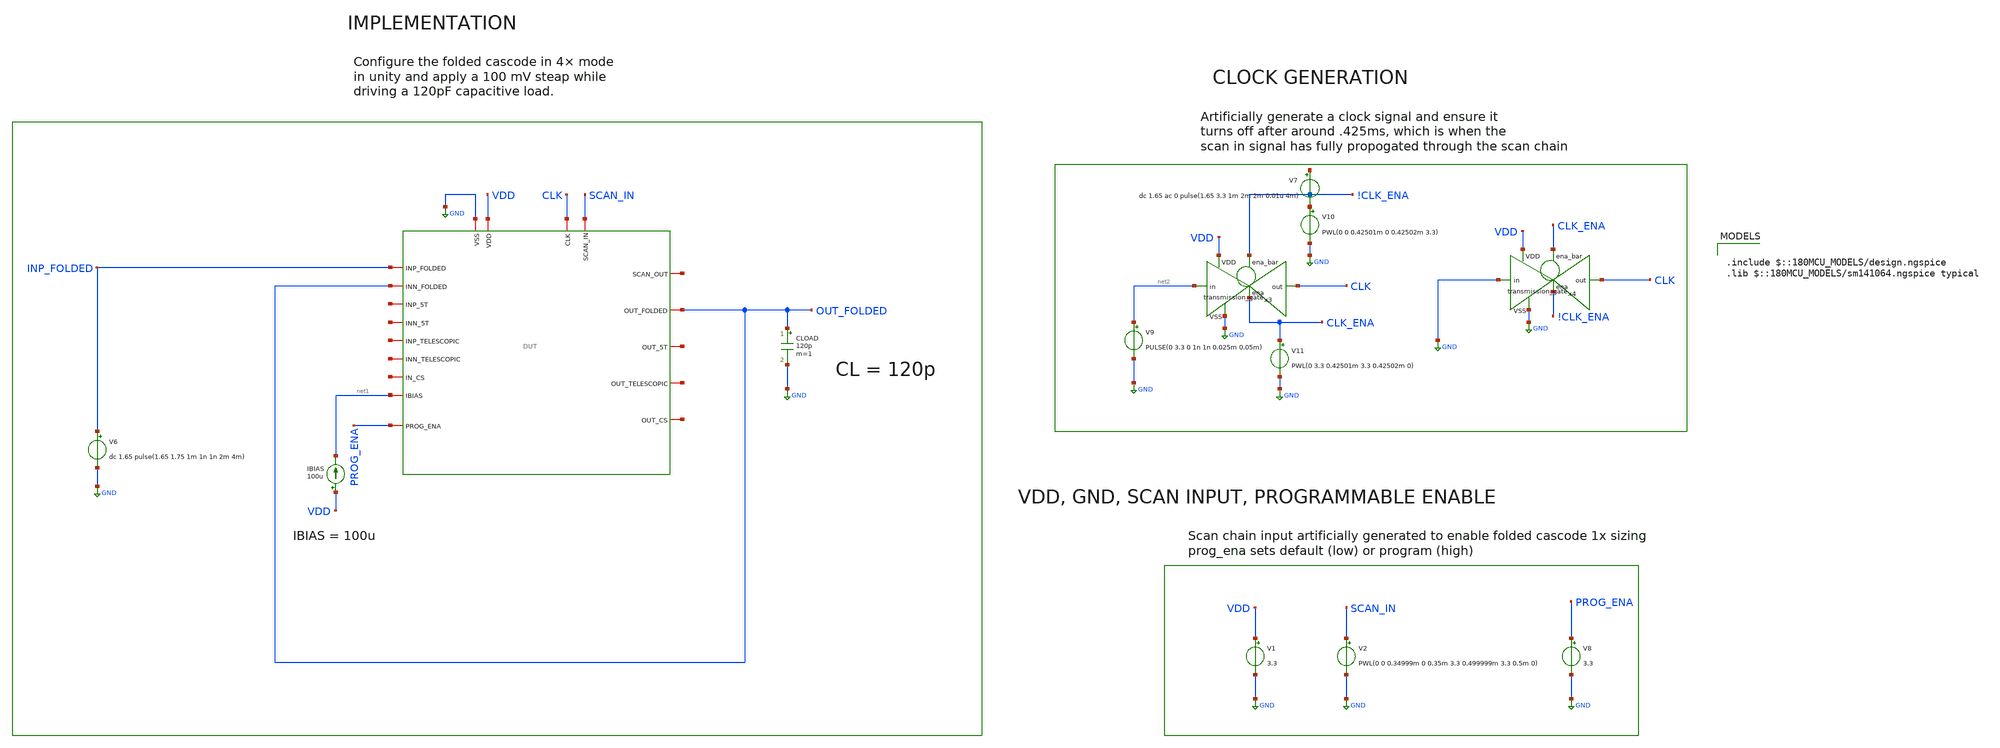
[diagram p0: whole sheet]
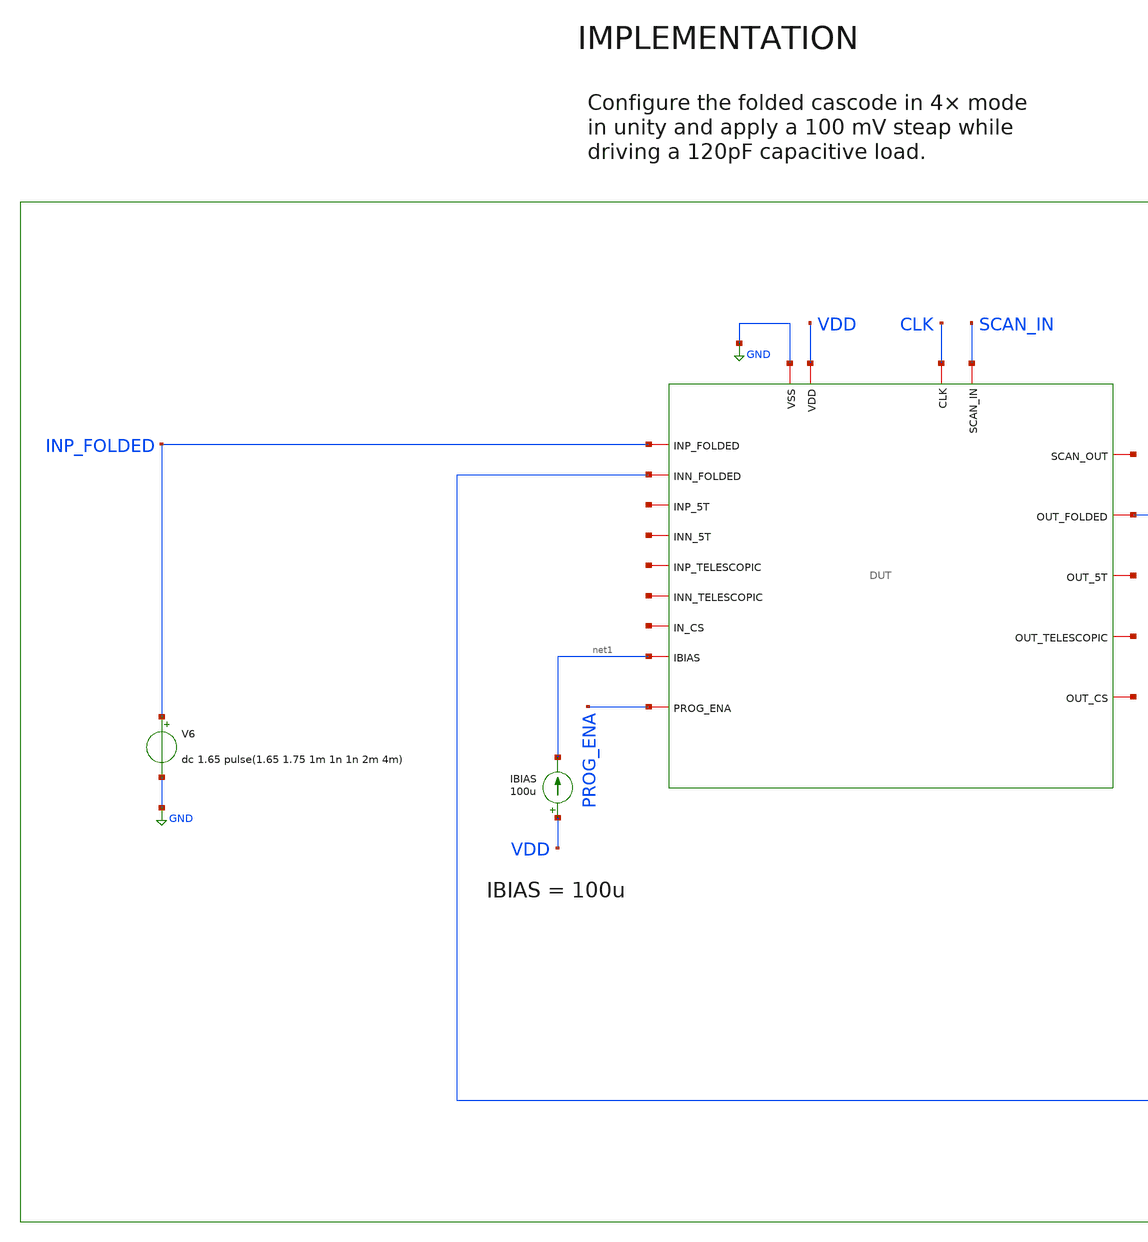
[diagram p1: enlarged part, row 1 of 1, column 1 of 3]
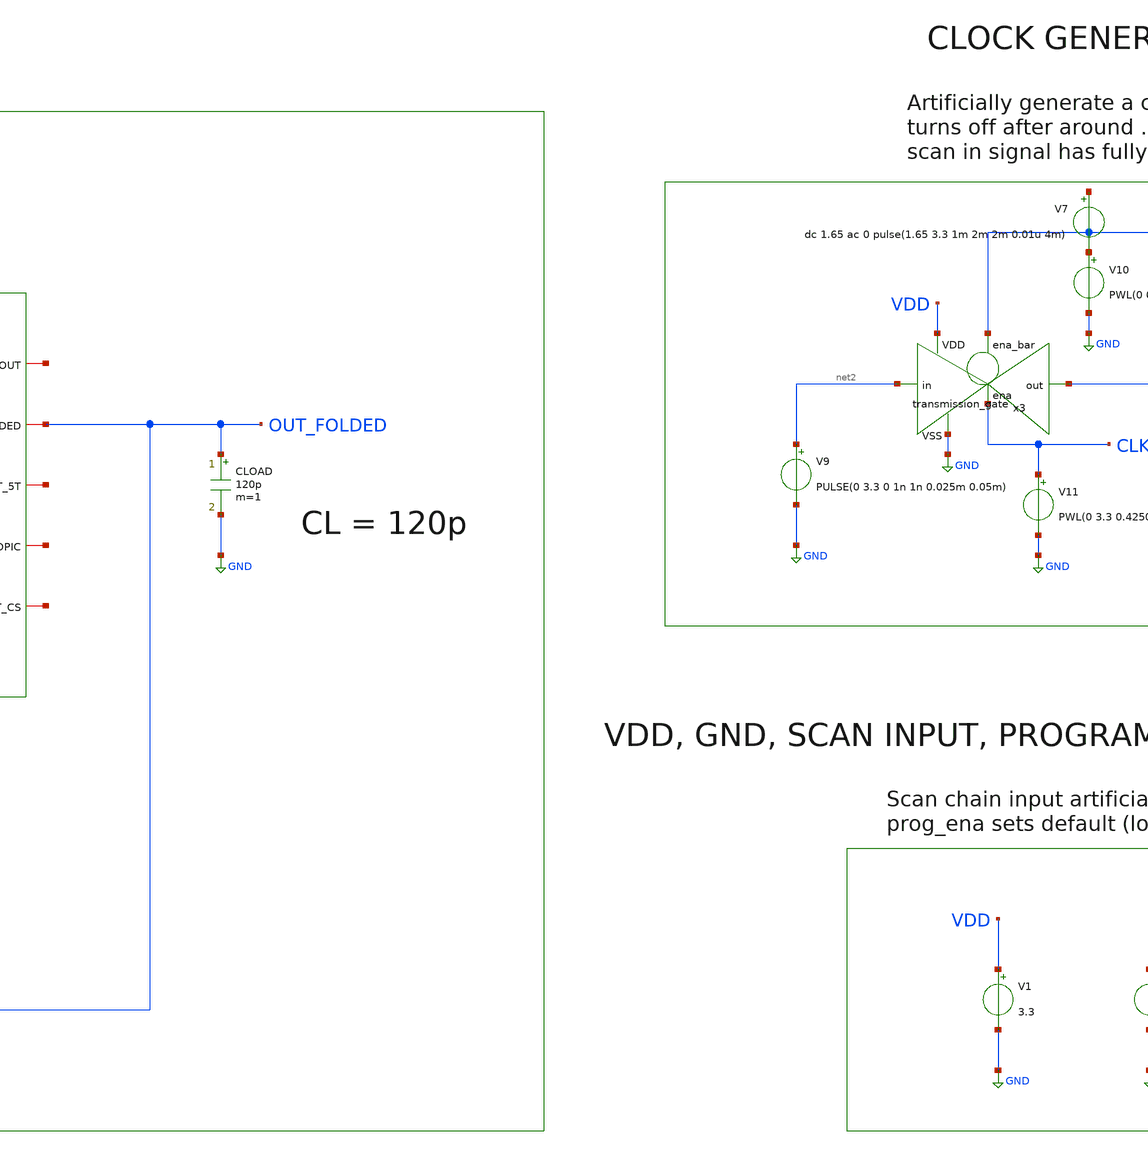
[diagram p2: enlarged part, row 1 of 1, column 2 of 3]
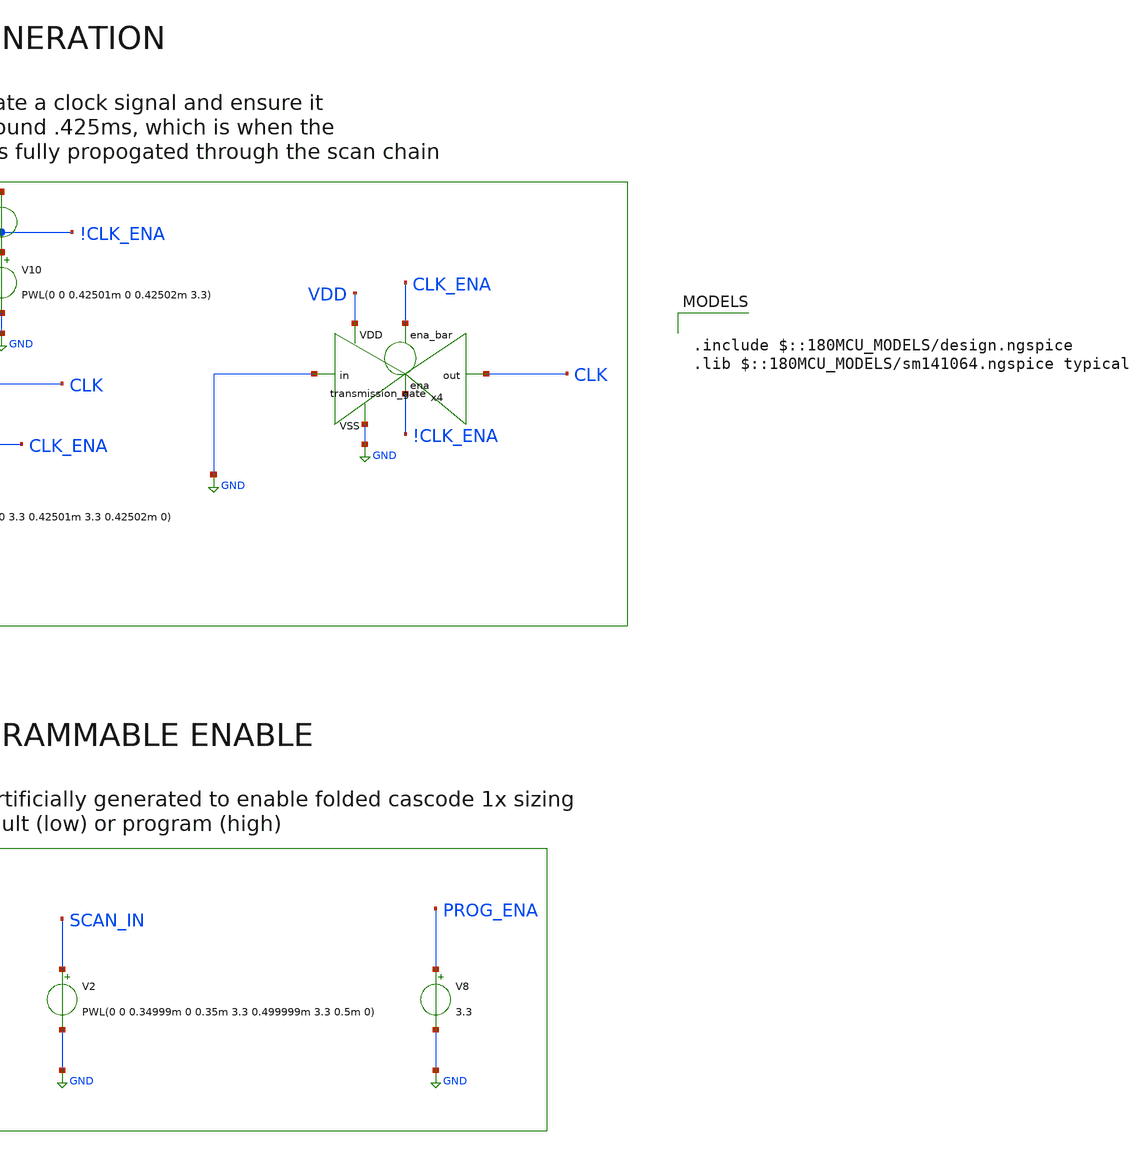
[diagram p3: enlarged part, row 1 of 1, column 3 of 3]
** sch_path: designs/libs/pex/folded/step_response/4x.sch
**.subckt 4x
V1 VDD GND 3.3
IBIAS VDD net1 100u
CLOAD OUT_FOLDED GND 120p m=1
V8 PROG_ENA GND 3.3
V9 net2 GND PULSE(0 3.3 0 1n 1n 0.025m 0.05m)
x3 !CLK_ENA VDD CLK net2 GND CLK_ENA transmission_gate
V10 !CLK_ENA GND PWL(0 0 0.42501m 0 0.42502m 3.3)
V11 CLK_ENA GND PWL(0 3.3 0.42501m 3.3 0.42502m 0)
x4 CLK_ENA VDD CLK GND GND !CLK_ENA transmission_gate
V6 INP_FOLDED GND dc 1.65 pulse(1.65 1.75 1m 1n 1n 2m 4m)
V2 SCAN_IN GND PWL(0 0 0.34999m 0 0.35m 3.3 0.499999m 3.3 0.5m 0)
V7 net3 !CLK_ENA dc 1.65 ac 0 pulse(1.65 3.3 1m 2m 2m 0.01u 4m)
x1 CLK net4 SCAN_IN GND VDD OUT_FOLDED INP_FOLDED net5 net1 OUT_FOLDED net6 net7 net8 net9 net10
+ net11 net12 PROG_ENA DUT
**** begin user architecture code

.include $::180MCU_MODELS/design.ngspice
.lib $::180MCU_MODELS/sm141064.ngspice typical



.include /foss/designs/libs/pex/DUT.spice
.control
tran 1u 5m

plot v(out_folded) v(inp_folded)

meas tran v_before find v(out_folded) at=0.99m
meas tran v_after find v(out_folded) at=2.5m

let delta = v_after - v_before
let t20_val = v_before + 0.2 * delta
let t80_val = v_before + 0.8 * delta

meas tran t_20 when v(out_folded) = t20_val rise = 1
meas tran t_80 when v(out_folded) = t80_val rise = 1
let sr_rise = delta / (t_80 - t_20)
print sr_rise

meas tran t_20f when v(out_folded) = t80_val fall = 1
meas tran t_80f when v(out_folded) = t20_val fall = 1
let sr_fall = delta / (t_80f - t_20f)
print sr_fall

meas tran vpeak max v(out_folded) from=1m to=3m
let overshoot = (vpeak - v_after) / delta * 100
print overshoot

meas tran t_settle when v(out_folded) = v_after td = 1m rise = 1
let settling = t_settle - 1m
print settling

print v_before v_after delta
.endc


**** end user architecture code
**.ends

* expanding   symbol:  libs/core_digital/schem/transmission_gate.sym # of pins=6
** sym_path: designs/libs/core_digital/schem/transmission_gate.sym
** sch_path: designs/libs/core_digital/schem/transmission_gate.sch
.subckt transmission_gate ena_bar VDD out in VSS ena
*.ipin in
*.ipin ena_bar
*.ipin ena
*.ipin VSS
*.ipin VDD
*.opin out
XM1 in ena_bar out VDD pfet_03v3 L=0.28u W=0.22u nf=1 ad='int((nf+1)/2) * W/nf * 0.18u' as='int((nf+2)/2) * W/nf * 0.18u'
+ pd='2*int((nf+1)/2) * (W/nf + 0.18u)' ps='2*int((nf+2)/2) * (W/nf + 0.18u)' nrd='0.18u / W' nrs='0.18u / W'
+ sa=0 sb=0 sd=0 m=1
XM2 in ena out VSS nfet_03v3 L=0.28u W=0.22u nf=1 ad='int((nf+1)/2) * W/nf * 0.18u' as='int((nf+2)/2) * W/nf * 0.18u'
+ pd='2*int((nf+1)/2) * (W/nf + 0.18u)' ps='2*int((nf+2)/2) * (W/nf + 0.18u)' nrd='0.18u / W' nrs='0.18u / W'
+ sa=0 sb=0 sd=0 m=1
.ends

.GLOBAL GND
.end
